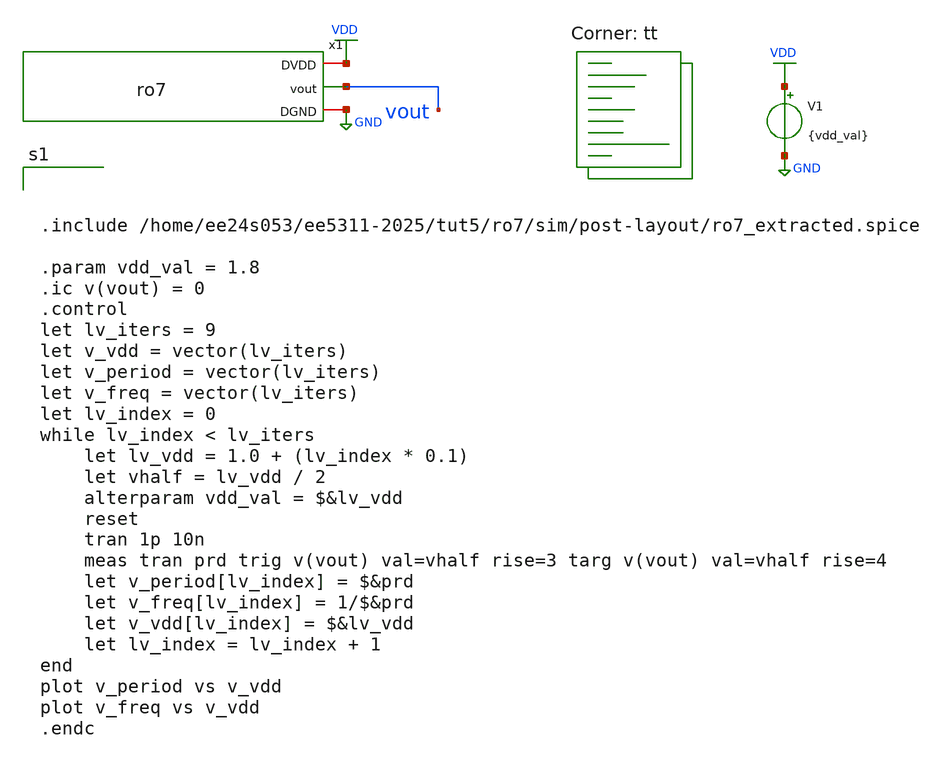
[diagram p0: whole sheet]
** sch_path: tut5/ro7/sim/post-layout/ro7_tb.sch
**.subckt ro7_tb
x1 VDD vout GND ro7
V1 VDD GND {vdd_val}
**** begin user architecture code



.include /home/ee24s053/ee5311-2025/tut5/ro7/sim/post-layout/ro7_extracted.spice

.param vdd_val = 1.8
.ic v(vout) = 0
.control
let lv_iters = 9
let v_vdd = vector(lv_iters)
let v_period = vector(lv_iters)
let v_freq = vector(lv_iters)
let lv_index = 0
while lv_index < lv_iters
	let lv_vdd = 1.0 + (lv_index * 0.1)
	let vhalf = lv_vdd / 2
	alterparam vdd_val = $&lv_vdd
	reset
	tran 1p 10n
	meas tran prd trig v(vout) val=vhalf rise=3 targ v(vout) val=vhalf rise=4
	let v_period[lv_index] = $&prd
	let v_freq[lv_index] = 1/$&prd
	let v_vdd[lv_index] = $&lv_vdd
	let lv_index = lv_index + 1
end
plot v_period vs v_vdd
plot v_freq vs v_vdd
.endc


.lib $::SKYWATER_MODELS/sky130.lib.spice tt
**** end user architecture code
**.ends
.GLOBAL VDD
.GLOBAL GND
.end
